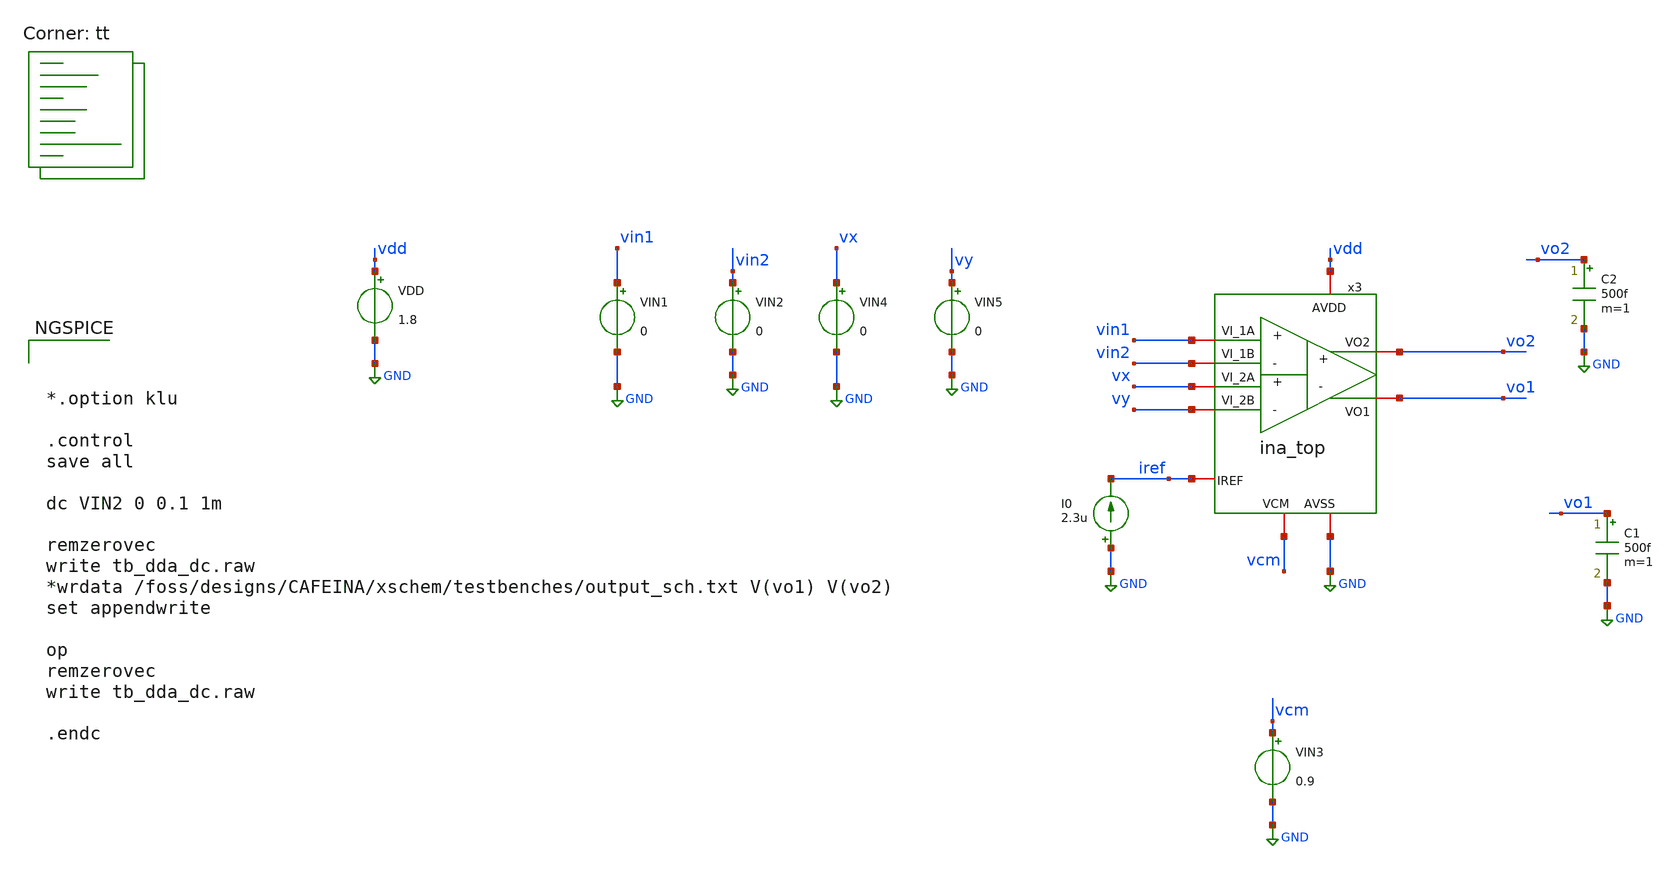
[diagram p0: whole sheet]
** sch_path: xschem/testbenches/tb_dda_dc.sch
**.subckt tb_dda_dc
VDD vdd GND 1.8
VIN1 vin1 GND 0
VIN2 vin2 GND 0
VIN3 vcm GND 0.9
I0 GND iref 2.3u
x3 vdd GND vin1 vin2 vo2 vo1 vcm iref vx vy ina_top
VIN4 vx GND 0
VIN5 vy GND 0
C1 vo1 GND 500f m=1
C2 vo2 GND 500f m=1
**** begin user architecture code



*.option klu

.control
save all

dc VIN2 0 0.1 1m

remzerovec
write tb_dda_dc.raw
*wrdata /foss/designs/CAFEINA/xschem/testbenches/output_sch.txt V(vo1) V(vo2)
set appendwrite

op
remzerovec
write tb_dda_dc.raw

.endc


.lib $::SKYWATER_MODELS/sky130.lib.spice tt
**** end user architecture code
**.ends
.GLOBAL GND
.end
